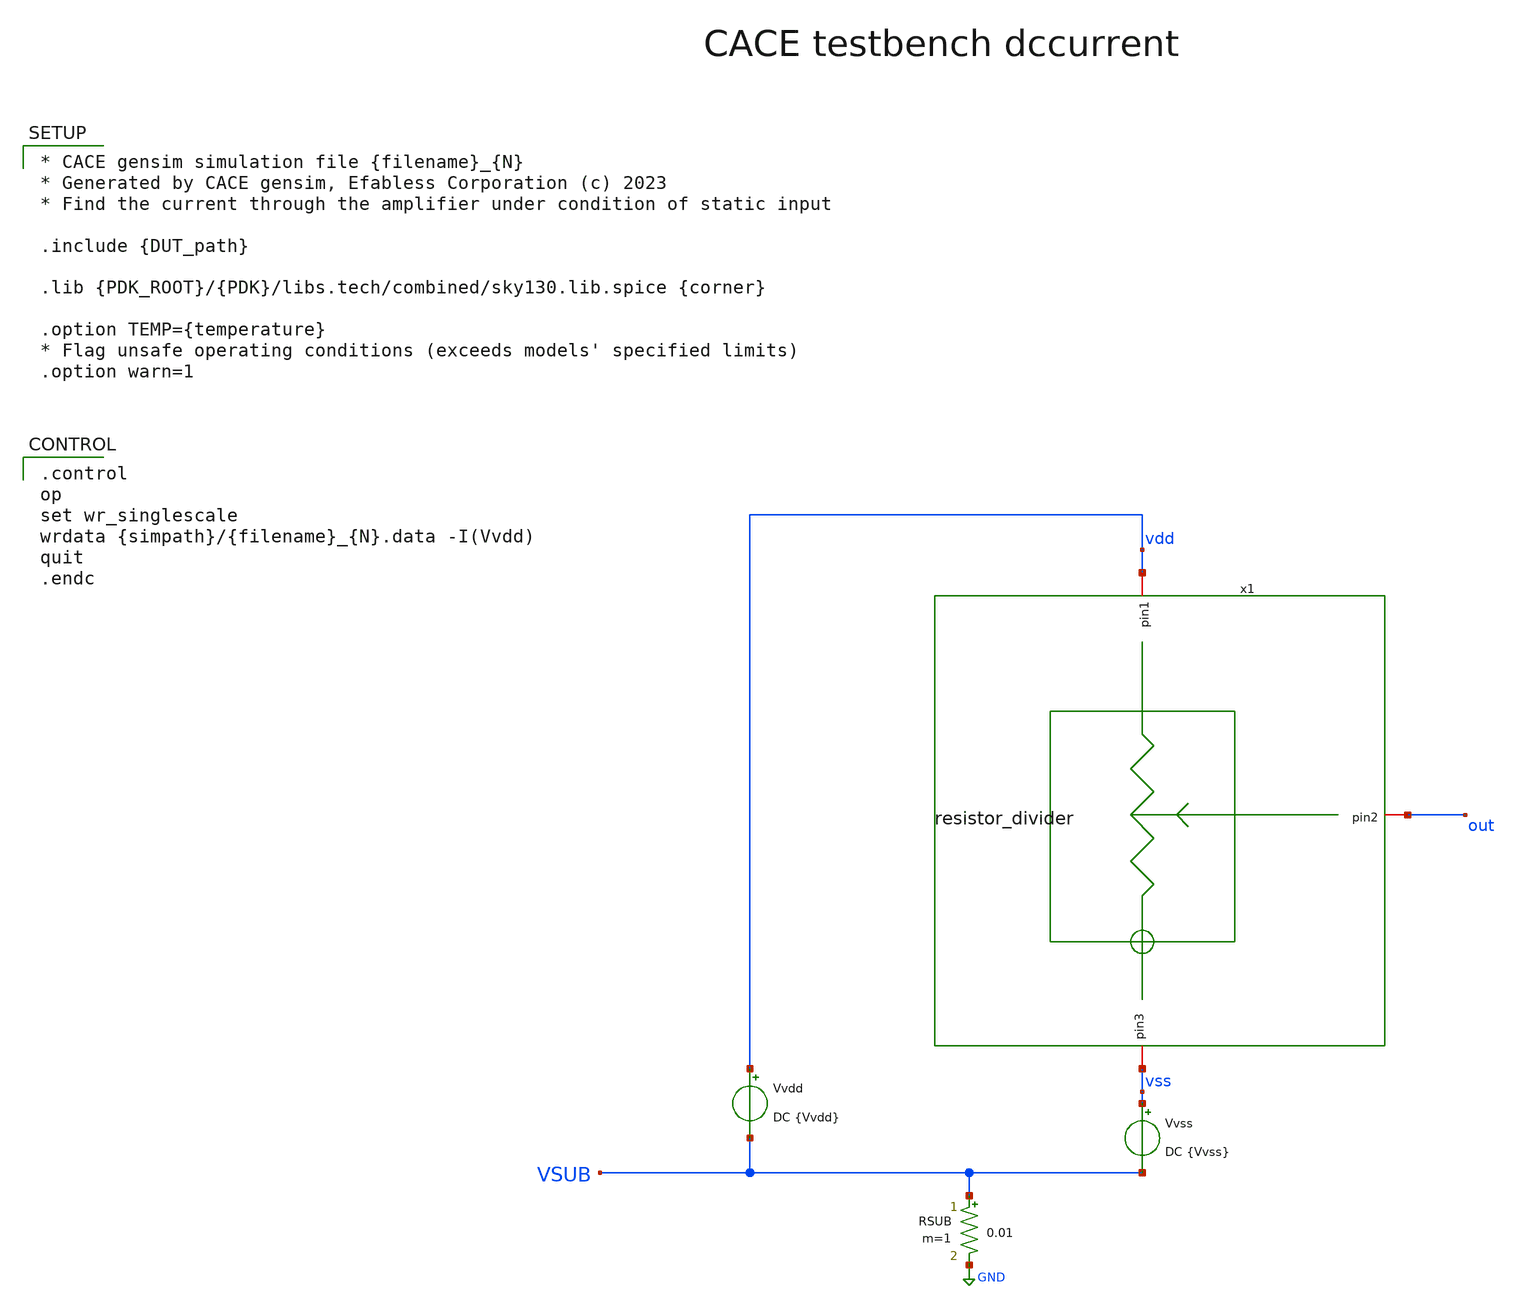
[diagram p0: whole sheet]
** sch_path: resistor_divider/cace/dccurrent.sch
**.subckt dccurrent
Vvdd vdd VSUB DC {Vvdd}
Vvss vss VSUB DC {Vvss}
RSUB VSUB GND 0.01 m=1
x1 vdd out vss resistor_divider
**** begin user architecture code

.control
op
set wr_singlescale
wrdata {simpath}/{filename}_{N}.data -I(Vvdd)
quit
.endc



* CACE gensim simulation file {filename}_{N}
* Generated by CACE gensim, Efabless Corporation (c) 2023
* Find the current through the amplifier under condition of static input

.include {DUT_path}

.lib {PDK_ROOT}/{PDK}/libs.tech/combined/sky130.lib.spice {corner}

.option TEMP={temperature}
* Flag unsafe operating conditions (exceeds models' specified limits)
.option warn=1


**** end user architecture code
**.ends

* expanding   symbol:  /home/sai/analog-tests/resistor_divider/xschem/resistor_divider.sym # of pins=3
** sym_path: resistor_divider/xschem/resistor_divider.sym
** sch_path: resistor_divider/xschem/resistor_divider.sch
.subckt resistor_divider pin1 pin2 pin3
*.iopin pin1
*.iopin pin3
*.iopin pin2
XR1 pin2 pin1 pin3 sky130_fd_pr__res_high_po_0p35 L=3.5 mult=1 m=1
XR2 pin3 pin2 pin3 sky130_fd_pr__res_high_po_0p35 L=3.5 mult=1 m=1
.ends

.GLOBAL GND
.end
